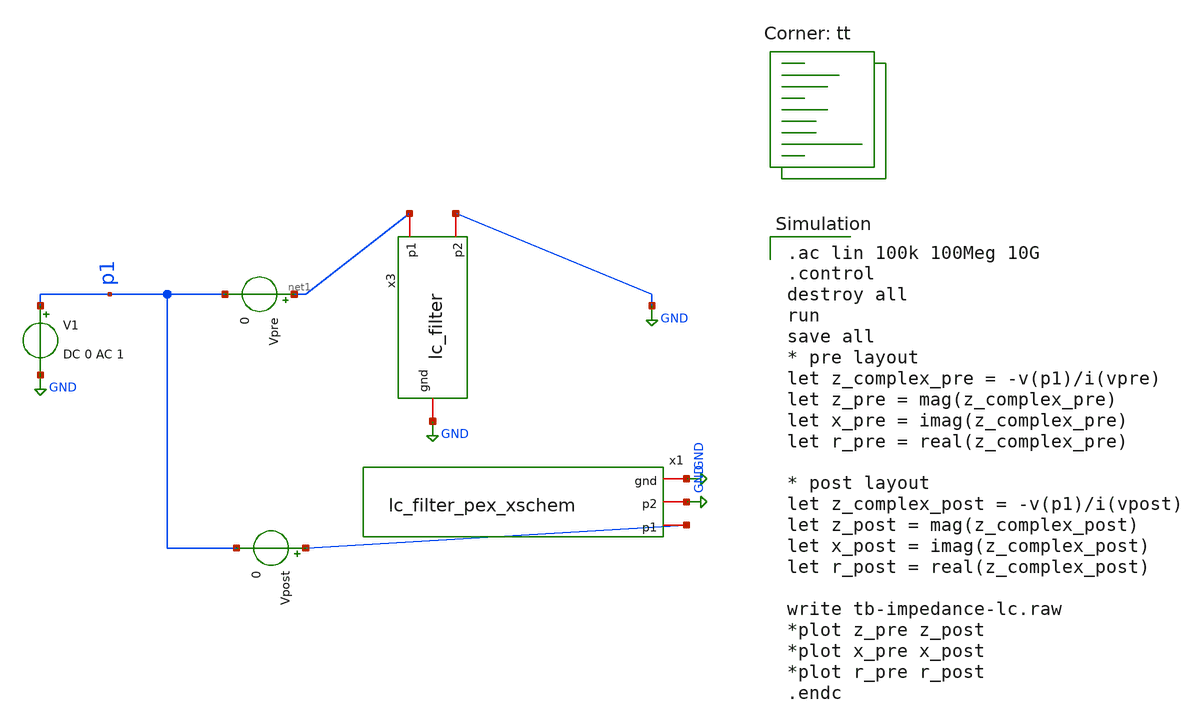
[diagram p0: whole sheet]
** sch_path: MICRO/tb-impedance-lc.sch
**.subckt tb-impedance-lc
V1 p1 GND DC 0 AC 1
Vpre net1 p1 0
Vpost net2 p1 0
x3 net1 GND GND lc_filter
x1 GND GND net2 lc_filter_pex_xschem
**** begin user architecture code

.ac lin 100k 100Meg 10G
.control
destroy all
run
save all
* pre layout
let z_complex_pre = -v(p1)/i(vpre)
let z_pre = mag(z_complex_pre)
let x_pre = imag(z_complex_pre)
let r_pre = real(z_complex_pre)

* post layout
let z_complex_post = -v(p1)/i(vpost)
let z_post = mag(z_complex_post)
let x_post = imag(z_complex_post)
let r_post = real(z_complex_post)

write tb-impedance-lc.raw
*plot z_pre z_post
*plot x_pre x_post
*plot r_pre r_post
.endc

.lib $::SKYWATER_MODELS/sky130.lib.spice tt
**** end user architecture code
**.ends
.GLOBAL GND
.end
